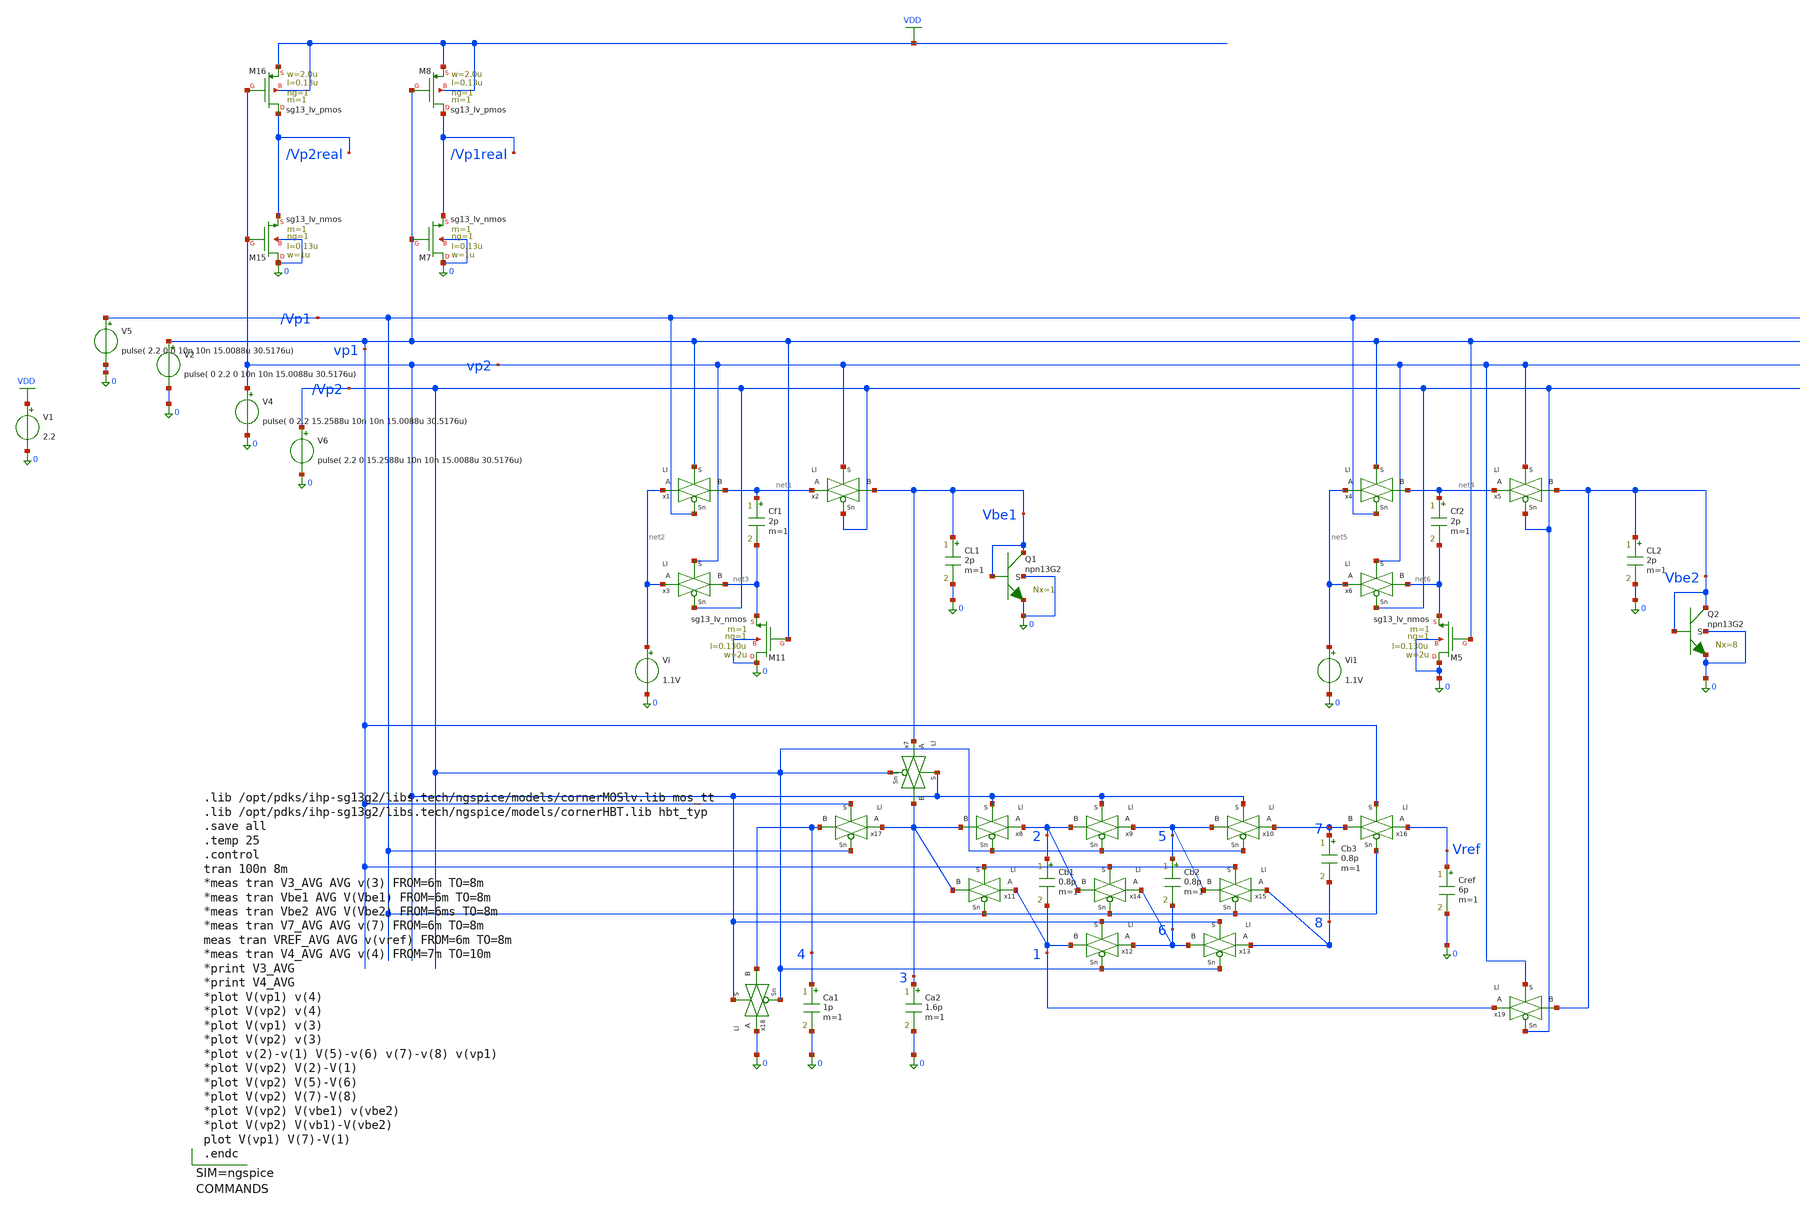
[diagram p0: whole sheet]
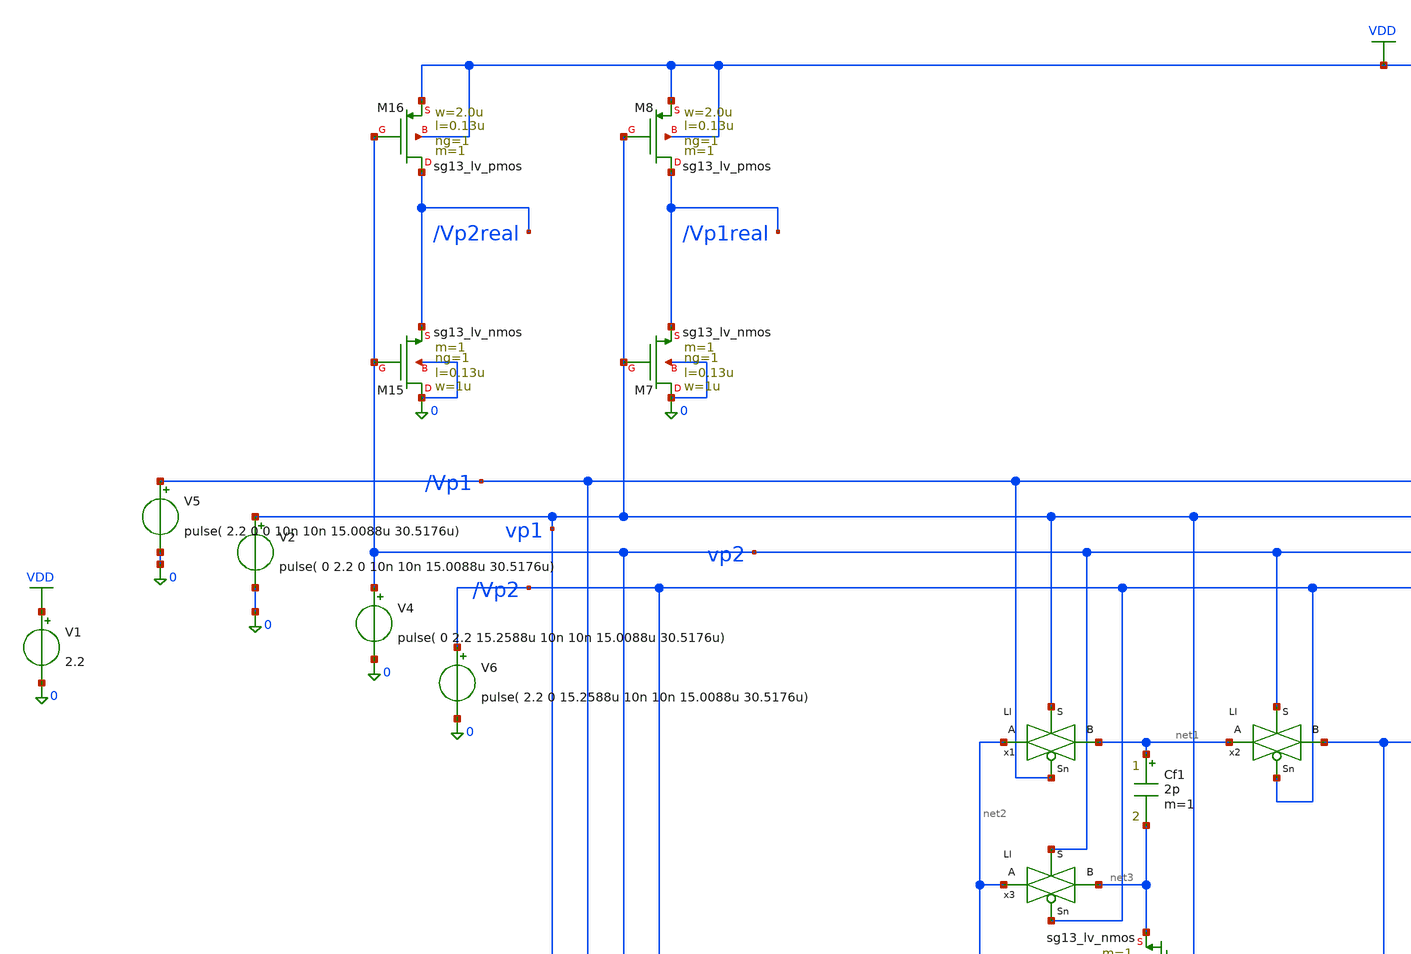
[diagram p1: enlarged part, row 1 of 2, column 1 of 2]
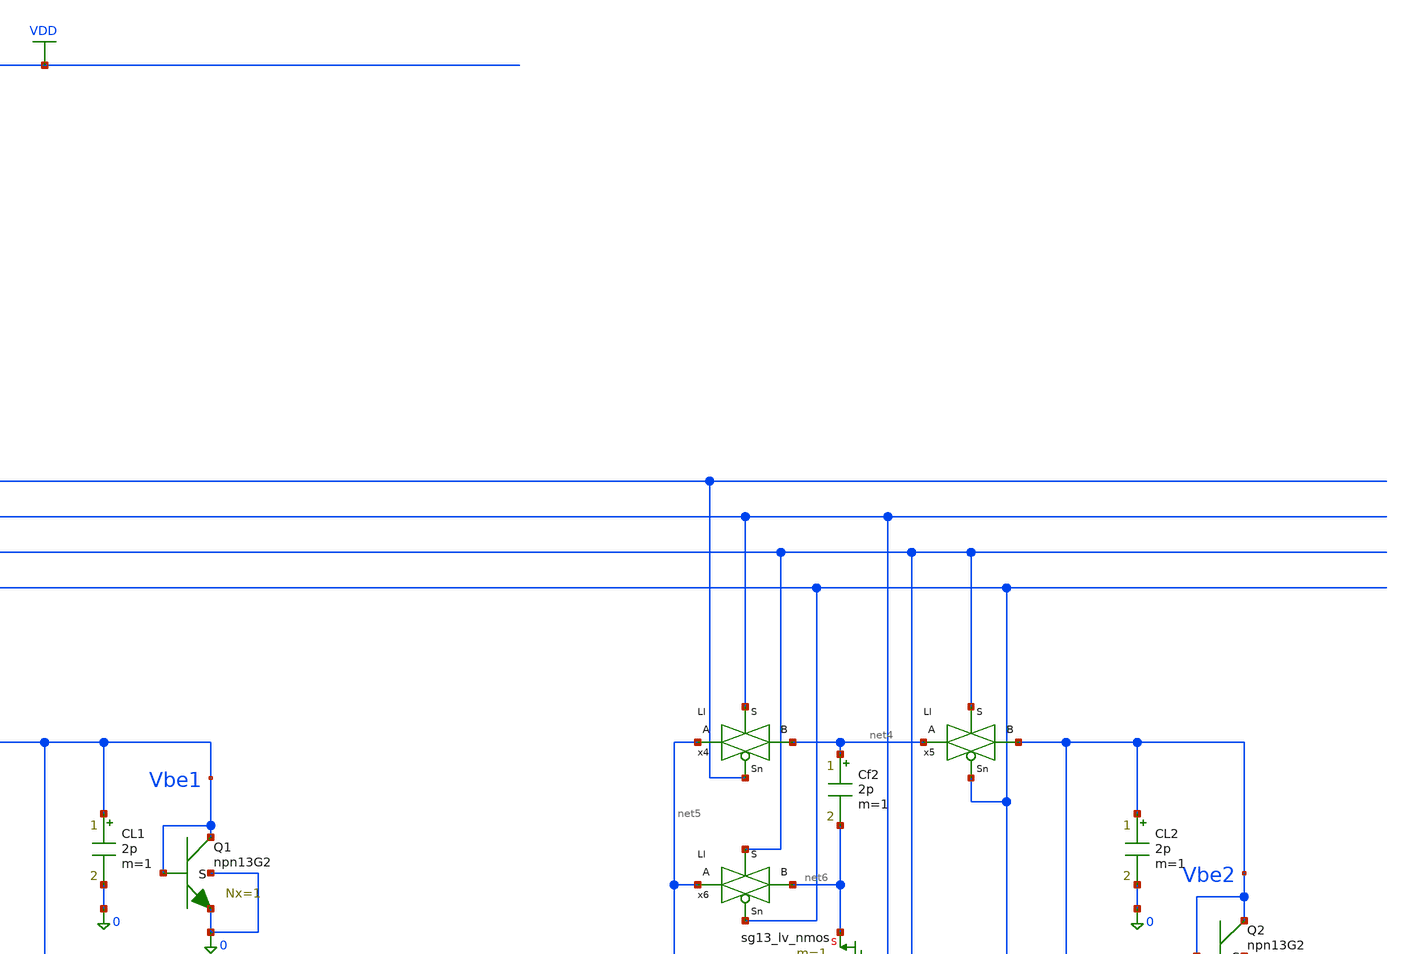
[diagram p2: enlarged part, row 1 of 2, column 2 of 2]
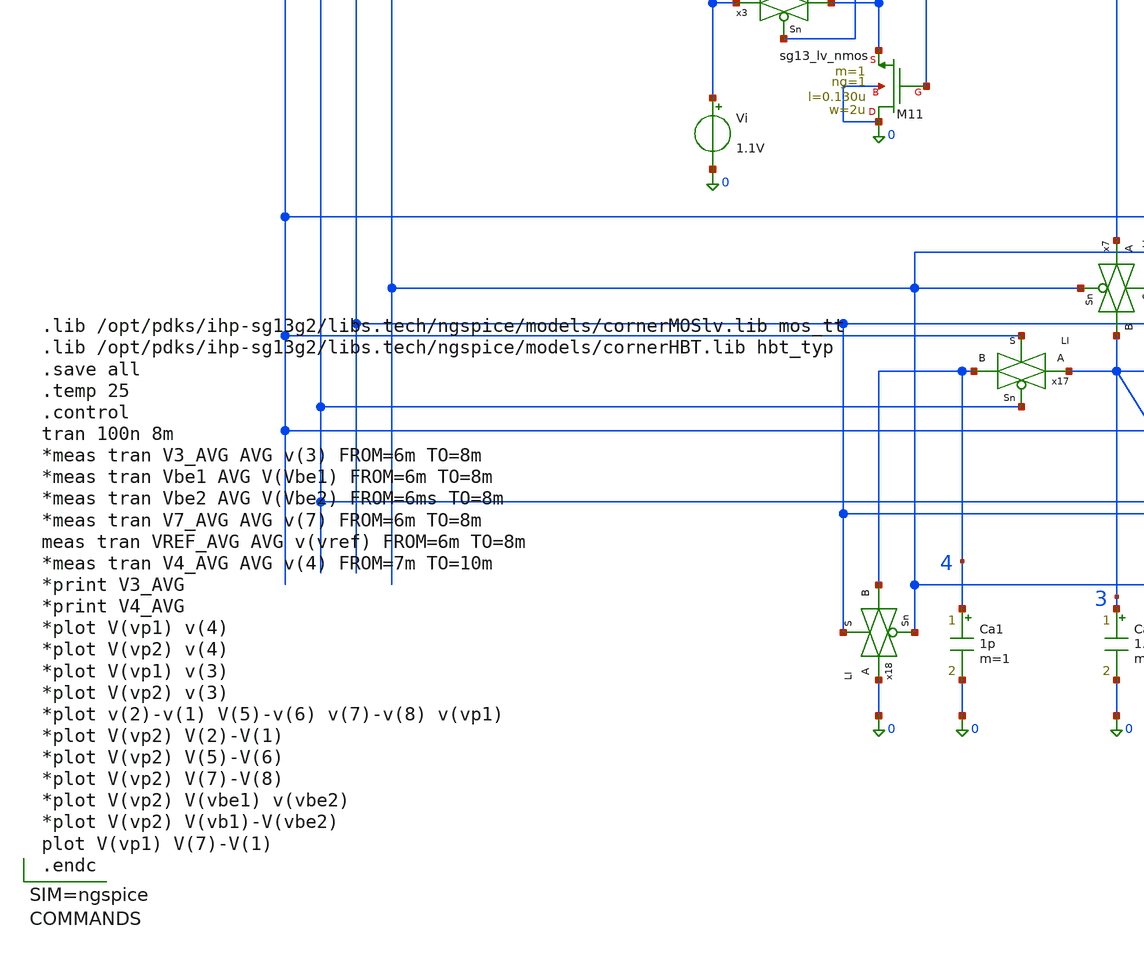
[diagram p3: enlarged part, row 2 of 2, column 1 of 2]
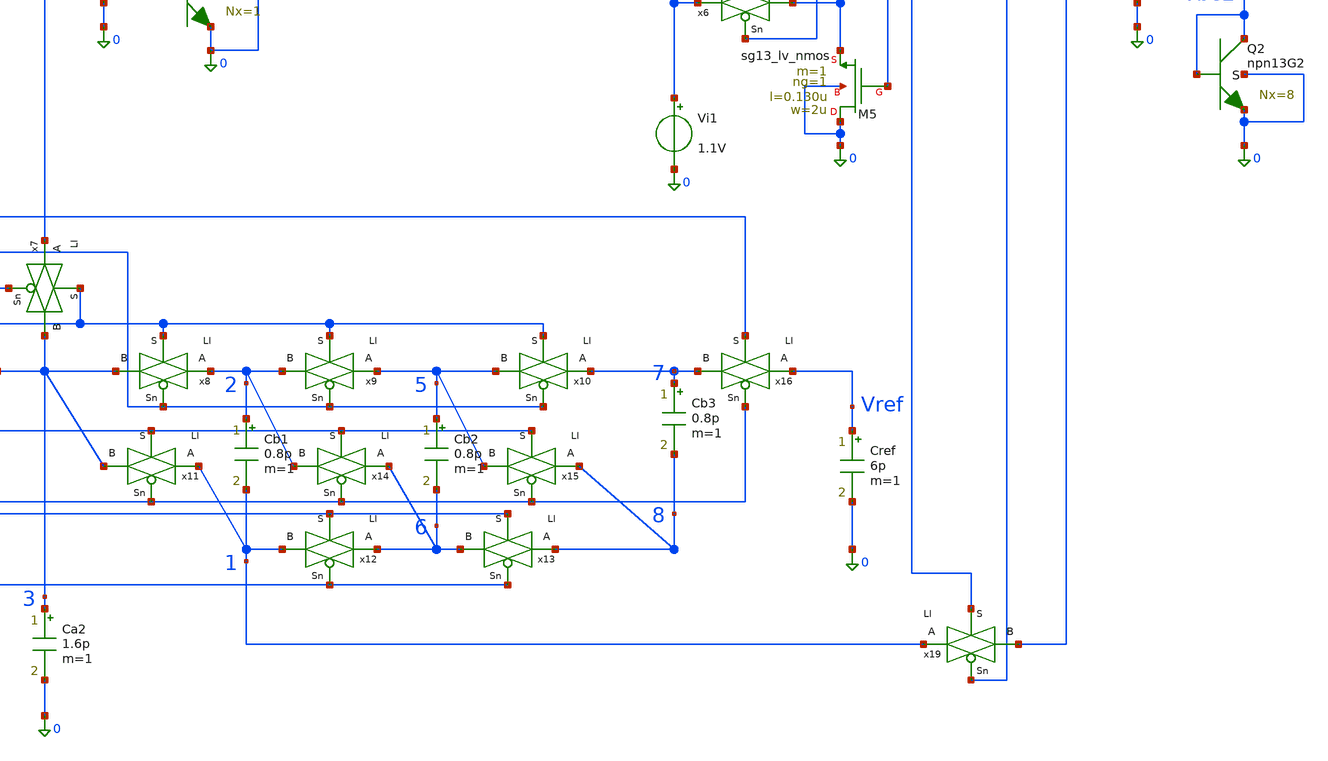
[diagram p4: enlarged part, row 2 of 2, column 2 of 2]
** sch_path: Enfoque_A/xschem/Bandgap_ISSCC5.sch
**.subckt Bandgap_ISSCC5
V1 VDD 0 2.2
XQ1 Vbe1 Vbe1 0 0 npn13G2 Nx=1 mm_ok=1
XQ2 Vbe2 Vbe2 0 0 npn13G2 Nx=8 mm_ok=1
V2 vp1 0 pulse( 0 2.2 0 10n 10n 15.0088u 30.5176u)
V4 vp2 0 pulse( 0 2.2 15.2588u 10n 10n 15.0088u 30.5176u)
Vi net2 0 1.1V
XM11 0 vp1 net3 0 sg13_lv_nmos w=2u l=0.130u ng=1 m=1 mm_ok=1
Cf1 net1 net3 2p m=1
CL1 Vbe1 0 2p m=1
XM7 0 vp1 /Vp1real 0 sg13_lv_nmos w=1u l=0.13u ng=1 m=1 mm_ok=1
XM8 /Vp1real vp1 VDD VDD sg13_lv_pmos w=2.0u l=0.13u ng=1 m=1 mm_ok=1
XM15 0 vp2 /Vp2real 0 sg13_lv_nmos w=1u l=0.13u ng=1 m=1 mm_ok=1
XM16 /Vp2real vp2 VDD VDD sg13_lv_pmos w=2.0u l=0.13u ng=1 m=1 mm_ok=1
x1 net2 net1 vp1 /Vp1 Ll
x2 net1 Vbe1 vp2 /Vp2 Ll
x3 net2 net3 vp2 /Vp2 Ll
V5 /Vp1 0 pulse( 2.2 0 0 10n 10n 15.0088u 30.5176u)
V6 /Vp2 0 pulse( 2.2 0 15.2588u 10n 10n 15.0088u 30.5176u)
Vi1 net5 0 1.1V
XM5 0 vp1 net6 0 sg13_lv_nmos w=2u l=0.130u ng=1 m=1 mm_ok=1
Cf2 net4 net6 2p m=1
CL2 Vbe2 0 2p m=1
x4 net5 net4 vp1 /Vp1 Ll
x5 net4 Vbe2 vp2 /Vp2 Ll
x6 net5 net6 vp2 /Vp2 Ll
x7 Vbe1 3 vp2 /Vp2 Ll
Ca2 3 0 1.6p m=1
x8 2 3 vp2 /Vp2 Ll
x9 5 2 vp2 /Vp2 Ll
x10 7 5 vp2 /Vp2 Ll
Cb1 2 1 0.8p m=1
x11 1 3 vp1 /Vp1 Ll
x12 6 1 vp2 /Vp2 Ll
x13 8 6 vp2 /Vp2 Ll
x14 6 2 vp1 /Vp1 Ll
x15 8 5 vp1 /Vp1 Ll
Cb2 5 6 0.8p m=1
Cb3 7 8 0.8p m=1
Cref Vref 0 6p m=1
x16 Vref 7 vp1 /Vp1 Ll
x17 3 4 vp1 /Vp1 Ll
x18 0 4 vp2 /Vp2 Ll
Ca1 4 0 1p m=1
x19 1 Vbe2 vp2 /Vp2 Ll
**** begin user architecture code


.lib /opt/pdks/ihp-sg13g2/libs.tech/ngspice/models/cornerMOSlv.lib mos_tt
.lib /opt/pdks/ihp-sg13g2/libs.tech/ngspice/models/cornerHBT.lib hbt_typ
.save all
.temp 25
.control
tran 100n 8m
*meas tran V3_AVG AVG v(3) FROM=6m TO=8m
*meas tran Vbe1 AVG V(Vbe1) FROM=6m TO=8m
*meas tran Vbe2 AVG V(Vbe2) FROM=6ms TO=8m
*meas tran V7_AVG AVG v(7) FROM=6m TO=8m
meas tran VREF_AVG AVG v(vref) FROM=6m TO=8m
*meas tran V4_AVG AVG v(4) FROM=7m TO=10m
*print V3_AVG
*print V4_AVG
*plot V(vp1) v(4)
*plot V(vp2) v(4)
*plot V(vp1) v(3)
*plot V(vp2) v(3)
*plot v(2)-v(1) V(5)-v(6) v(7)-v(8) v(vp1)
*plot V(vp2) V(2)-V(1)
*plot V(vp2) V(5)-V(6)
*plot V(vp2) V(7)-V(8)
*plot V(vp2) V(vbe1) v(vbe2)
*plot V(vp2) V(vb1)-V(vbe2)
plot V(vp1) V(7)-V(1)
.endc



**** end user architecture code
**.ends
.GLOBAL VDD
.end
